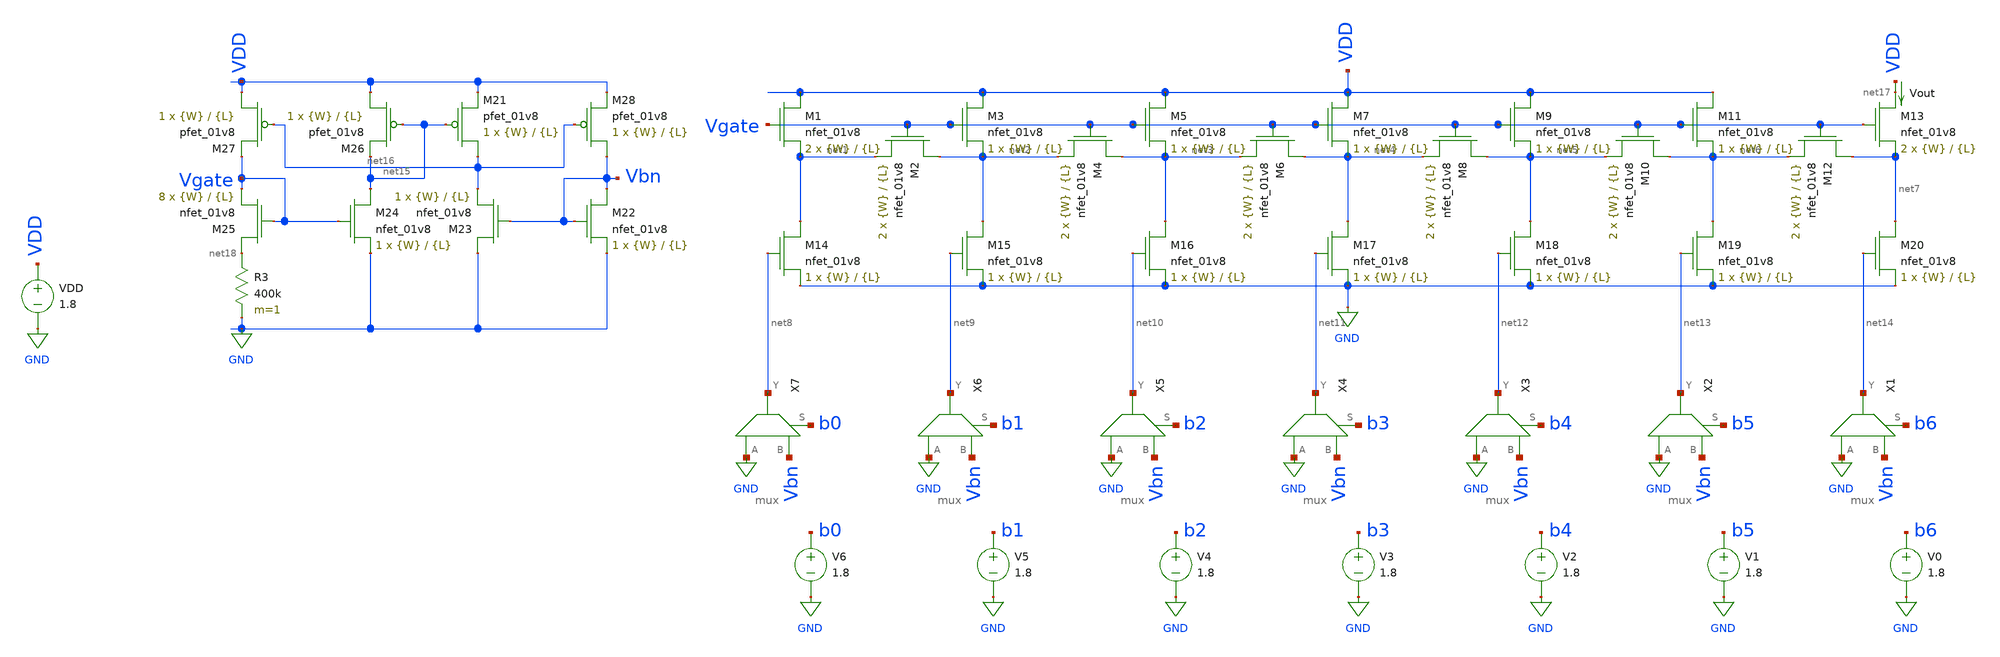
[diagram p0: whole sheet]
** sch_path: dac/schematics/misc/dac_output_current.sch
**.subckt dac_output_current
XM1 VDD Vgate net1 GND sky130_fd_pr__nfet_01v8 L={L} W={W} nf=1 ad='int((nf+1)/2) * W/nf * 0.29' as='int((nf+2)/2) * W/nf * 0.29'
+ pd='2*int((nf+1)/2) * (W/nf + 0.29)' ps='2*int((nf+2)/2) * (W/nf + 0.29)' nrd='0.29 / W' nrs='0.29 / W'
+ sa=0 sb=0 sd=0 mult=2 m=2
XM2 net2 Vgate net1 GND sky130_fd_pr__nfet_01v8 L={L} W={W} nf=1 ad='int((nf+1)/2) * W/nf * 0.29' as='int((nf+2)/2) * W/nf * 0.29'
+ pd='2*int((nf+1)/2) * (W/nf + 0.29)' ps='2*int((nf+2)/2) * (W/nf + 0.29)' nrd='0.29 / W' nrs='0.29 / W'
+ sa=0 sb=0 sd=0 mult=2 m=2
XM3 VDD Vgate net2 GND sky130_fd_pr__nfet_01v8 L={L} W={W} nf=1 ad='int((nf+1)/2) * W/nf * 0.29' as='int((nf+2)/2) * W/nf * 0.29'
+ pd='2*int((nf+1)/2) * (W/nf + 0.29)' ps='2*int((nf+2)/2) * (W/nf + 0.29)' nrd='0.29 / W' nrs='0.29 / W'
+ sa=0 sb=0 sd=0 mult=1 m=1
XM4 net3 Vgate net2 GND sky130_fd_pr__nfet_01v8 L={L} W={W} nf=1 ad='int((nf+1)/2) * W/nf * 0.29' as='int((nf+2)/2) * W/nf * 0.29'
+ pd='2*int((nf+1)/2) * (W/nf + 0.29)' ps='2*int((nf+2)/2) * (W/nf + 0.29)' nrd='0.29 / W' nrs='0.29 / W'
+ sa=0 sb=0 sd=0 mult=2 m=2
XM5 VDD Vgate net3 GND sky130_fd_pr__nfet_01v8 L={L} W={W} nf=1 ad='int((nf+1)/2) * W/nf * 0.29' as='int((nf+2)/2) * W/nf * 0.29'
+ pd='2*int((nf+1)/2) * (W/nf + 0.29)' ps='2*int((nf+2)/2) * (W/nf + 0.29)' nrd='0.29 / W' nrs='0.29 / W'
+ sa=0 sb=0 sd=0 mult=1 m=1
XM6 net4 Vgate net3 GND sky130_fd_pr__nfet_01v8 L={L} W={W} nf=1 ad='int((nf+1)/2) * W/nf * 0.29' as='int((nf+2)/2) * W/nf * 0.29'
+ pd='2*int((nf+1)/2) * (W/nf + 0.29)' ps='2*int((nf+2)/2) * (W/nf + 0.29)' nrd='0.29 / W' nrs='0.29 / W'
+ sa=0 sb=0 sd=0 mult=2 m=2
XM7 VDD Vgate net4 GND sky130_fd_pr__nfet_01v8 L={L} W={W} nf=1 ad='int((nf+1)/2) * W/nf * 0.29' as='int((nf+2)/2) * W/nf * 0.29'
+ pd='2*int((nf+1)/2) * (W/nf + 0.29)' ps='2*int((nf+2)/2) * (W/nf + 0.29)' nrd='0.29 / W' nrs='0.29 / W'
+ sa=0 sb=0 sd=0 mult=1 m=1
XM8 net5 Vgate net4 GND sky130_fd_pr__nfet_01v8 L={L} W={W} nf=1 ad='int((nf+1)/2) * W/nf * 0.29' as='int((nf+2)/2) * W/nf * 0.29'
+ pd='2*int((nf+1)/2) * (W/nf + 0.29)' ps='2*int((nf+2)/2) * (W/nf + 0.29)' nrd='0.29 / W' nrs='0.29 / W'
+ sa=0 sb=0 sd=0 mult=2 m=2
XM9 VDD Vgate net5 GND sky130_fd_pr__nfet_01v8 L={L} W={W} nf=1 ad='int((nf+1)/2) * W/nf * 0.29' as='int((nf+2)/2) * W/nf * 0.29'
+ pd='2*int((nf+1)/2) * (W/nf + 0.29)' ps='2*int((nf+2)/2) * (W/nf + 0.29)' nrd='0.29 / W' nrs='0.29 / W'
+ sa=0 sb=0 sd=0 mult=1 m=1
XM10 net6 Vgate net5 GND sky130_fd_pr__nfet_01v8 L={L} W={W} nf=1 ad='int((nf+1)/2) * W/nf * 0.29' as='int((nf+2)/2) * W/nf * 0.29'
+ pd='2*int((nf+1)/2) * (W/nf + 0.29)' ps='2*int((nf+2)/2) * (W/nf + 0.29)' nrd='0.29 / W' nrs='0.29 / W'
+ sa=0 sb=0 sd=0 mult=2 m=2
XM11 VDD Vgate net6 GND sky130_fd_pr__nfet_01v8 L={L} W={W} nf=1 ad='int((nf+1)/2) * W/nf * 0.29' as='int((nf+2)/2) * W/nf * 0.29'
+ pd='2*int((nf+1)/2) * (W/nf + 0.29)' ps='2*int((nf+2)/2) * (W/nf + 0.29)' nrd='0.29 / W' nrs='0.29 / W'
+ sa=0 sb=0 sd=0 mult=1 m=1
XM12 net7 Vgate net6 GND sky130_fd_pr__nfet_01v8 L={L} W={W} nf=1 ad='int((nf+1)/2) * W/nf * 0.29' as='int((nf+2)/2) * W/nf * 0.29'
+ pd='2*int((nf+1)/2) * (W/nf + 0.29)' ps='2*int((nf+2)/2) * (W/nf + 0.29)' nrd='0.29 / W' nrs='0.29 / W'
+ sa=0 sb=0 sd=0 mult=2 m=2
XM13 net17 Vgate net7 GND sky130_fd_pr__nfet_01v8 L={L} W={W} nf=1 ad='int((nf+1)/2) * W/nf * 0.29' as='int((nf+2)/2) * W/nf * 0.29'
+ pd='2*int((nf+1)/2) * (W/nf + 0.29)' ps='2*int((nf+2)/2) * (W/nf + 0.29)' nrd='0.29 / W' nrs='0.29 / W'
+ sa=0 sb=0 sd=0 mult=2 m=2
XM14 net1 net8 GND GND sky130_fd_pr__nfet_01v8 L={L} W={W} nf=1 ad='int((nf+1)/2) * W/nf * 0.29' as='int((nf+2)/2) * W/nf * 0.29'
+ pd='2*int((nf+1)/2) * (W/nf + 0.29)' ps='2*int((nf+2)/2) * (W/nf + 0.29)' nrd='0.29 / W' nrs='0.29 / W'
+ sa=0 sb=0 sd=0 mult=1 m=1
XM15 net2 net9 GND GND sky130_fd_pr__nfet_01v8 L={L} W={W} nf=1 ad='int((nf+1)/2) * W/nf * 0.29' as='int((nf+2)/2) * W/nf * 0.29'
+ pd='2*int((nf+1)/2) * (W/nf + 0.29)' ps='2*int((nf+2)/2) * (W/nf + 0.29)' nrd='0.29 / W' nrs='0.29 / W'
+ sa=0 sb=0 sd=0 mult=1 m=1
XM16 net3 net10 GND GND sky130_fd_pr__nfet_01v8 L={L} W={W} nf=1 ad='int((nf+1)/2) * W/nf * 0.29' as='int((nf+2)/2) * W/nf * 0.29'
+ pd='2*int((nf+1)/2) * (W/nf + 0.29)' ps='2*int((nf+2)/2) * (W/nf + 0.29)' nrd='0.29 / W' nrs='0.29 / W'
+ sa=0 sb=0 sd=0 mult=1 m=1
XM17 net4 net11 GND GND sky130_fd_pr__nfet_01v8 L={L} W={W} nf=1 ad='int((nf+1)/2) * W/nf * 0.29' as='int((nf+2)/2) * W/nf * 0.29'
+ pd='2*int((nf+1)/2) * (W/nf + 0.29)' ps='2*int((nf+2)/2) * (W/nf + 0.29)' nrd='0.29 / W' nrs='0.29 / W'
+ sa=0 sb=0 sd=0 mult=1 m=1
XM18 net5 net12 GND GND sky130_fd_pr__nfet_01v8 L={L} W={W} nf=1 ad='int((nf+1)/2) * W/nf * 0.29' as='int((nf+2)/2) * W/nf * 0.29'
+ pd='2*int((nf+1)/2) * (W/nf + 0.29)' ps='2*int((nf+2)/2) * (W/nf + 0.29)' nrd='0.29 / W' nrs='0.29 / W'
+ sa=0 sb=0 sd=0 mult=1 m=1
XM19 net6 net13 GND GND sky130_fd_pr__nfet_01v8 L={L} W={W} nf=1 ad='int((nf+1)/2) * W/nf * 0.29' as='int((nf+2)/2) * W/nf * 0.29'
+ pd='2*int((nf+1)/2) * (W/nf + 0.29)' ps='2*int((nf+2)/2) * (W/nf + 0.29)' nrd='0.29 / W' nrs='0.29 / W'
+ sa=0 sb=0 sd=0 mult=1 m=1
XM20 net7 net14 GND GND sky130_fd_pr__nfet_01v8 L={L} W={W} nf=1 ad='int((nf+1)/2) * W/nf * 0.29' as='int((nf+2)/2) * W/nf * 0.29'
+ pd='2*int((nf+1)/2) * (W/nf + 0.29)' ps='2*int((nf+2)/2) * (W/nf + 0.29)' nrd='0.29 / W' nrs='0.29 / W'
+ sa=0 sb=0 sd=0 mult=1 m=1
X1 GND Vbn net14 b6 mux
X2 GND Vbn net13 b5 mux
X3 GND Vbn net12 b4 mux
X4 GND Vbn net11 b3 mux
X5 GND Vbn net10 b2 mux
X6 GND Vbn net9 b1 mux
X7 GND Vbn net8 b0 mux
V0 b6 GND 1.8
V1 b5 GND 1.8
V2 b4 GND 1.8
V3 b3 GND 1.8
V4 b2 GND 1.8
V5 b1 GND 1.8
V6 b0 GND 1.8
Vout VDD net17 0
.save i(vout)
VDD VDD GND 1.8
R3 net18 GND 400k m=1
XM28 Vbn net16 VDD VDD sky130_fd_pr__pfet_01v8 L={L} W={W} nf=1 ad='int((nf+1)/2) * W/nf * 0.29' as='int((nf+2)/2) * W/nf * 0.29'
+ pd='2*int((nf+1)/2) * (W/nf + 0.29)' ps='2*int((nf+2)/2) * (W/nf + 0.29)' nrd='0.29 / W' nrs='0.29 / W'
+ sa=0 sb=0 sd=0 mult=1 m=1
XM21 net16 net15 VDD VDD sky130_fd_pr__pfet_01v8 L={L} W={W} nf=1 ad='int((nf+1)/2) * W/nf * 0.29' as='int((nf+2)/2) * W/nf * 0.29'
+ pd='2*int((nf+1)/2) * (W/nf + 0.29)' ps='2*int((nf+2)/2) * (W/nf + 0.29)' nrd='0.29 / W' nrs='0.29 / W'
+ sa=0 sb=0 sd=0 mult=1 m=1
XM26 VDD net15 net15 VDD sky130_fd_pr__pfet_01v8 L={L} W={W} nf=1 ad='int((nf+1)/2) * W/nf * 0.29' as='int((nf+2)/2) * W/nf * 0.29'
+ pd='2*int((nf+1)/2) * (W/nf + 0.29)' ps='2*int((nf+2)/2) * (W/nf + 0.29)' nrd='0.29 / W' nrs='0.29 / W'
+ sa=0 sb=0 sd=0 mult=1 m=1
XM27 VDD net16 Vgate VDD sky130_fd_pr__pfet_01v8 L={L} W={W} nf=1 ad='int((nf+1)/2) * W/nf * 0.29' as='int((nf+2)/2) * W/nf * 0.29'
+ pd='2*int((nf+1)/2) * (W/nf + 0.29)' ps='2*int((nf+2)/2) * (W/nf + 0.29)' nrd='0.29 / W' nrs='0.29 / W'
+ sa=0 sb=0 sd=0 mult=1 m=1
XM22 Vbn Vbn GND GND sky130_fd_pr__nfet_01v8 L={L} W={W} nf=1 ad='int((nf+1)/2) * W/nf * 0.29' as='int((nf+2)/2) * W/nf * 0.29'
+ pd='2*int((nf+1)/2) * (W/nf + 0.29)' ps='2*int((nf+2)/2) * (W/nf + 0.29)' nrd='0.29 / W' nrs='0.29 / W'
+ sa=0 sb=0 sd=0 mult=1 m=1
XM23 GND Vbn net16 GND sky130_fd_pr__nfet_01v8 L={L} W={W} nf=1 ad='int((nf+1)/2) * W/nf * 0.29' as='int((nf+2)/2) * W/nf * 0.29'
+ pd='2*int((nf+1)/2) * (W/nf + 0.29)' ps='2*int((nf+2)/2) * (W/nf + 0.29)' nrd='0.29 / W' nrs='0.29 / W'
+ sa=0 sb=0 sd=0 mult=1 m=1
XM24 net15 Vgate GND GND sky130_fd_pr__nfet_01v8 L={L} W={W} nf=1 ad='int((nf+1)/2) * W/nf * 0.29' as='int((nf+2)/2) * W/nf * 0.29'
+ pd='2*int((nf+1)/2) * (W/nf + 0.29)' ps='2*int((nf+2)/2) * (W/nf + 0.29)' nrd='0.29 / W' nrs='0.29 / W'
+ sa=0 sb=0 sd=0 mult=1 m=1
XM25 net18 Vgate Vgate GND sky130_fd_pr__nfet_01v8 L={L} W={W} nf=1 ad='int((nf+1)/2) * W/nf * 0.29'
+ as='int((nf+2)/2) * W/nf * 0.29' pd='2*int((nf+1)/2) * (W/nf + 0.29)' ps='2*int((nf+2)/2) * (W/nf + 0.29)'
+ nrd='0.29 / W' nrs='0.29 / W' sa=0 sb=0 sd=0 mult=8 m=8
**** begin user architecture code

.param W=1
.param L=0.5
.dc VDD 0 1.8 0.01
.save i(Vout) v(VDD) v(Vbn) v(Vgate)


.option wnflag=1
.param MC_SWITCH=0.0
.lib ~/skywater/skywater-pdk/libraries/sky130_fd_pr_ngspice/latest/models/sky130.lib.spice tt

**** end user architecture code
**.ends

* expanding   symbol:  /home/madvlsi/Documents/current-output-dac-vlsi/schematics/mux.sym # of
*+ pins=4
** sym_path: dac/schematics/mux.sym
** sch_path: dac/schematics/mux.sch
.subckt mux A B Y S
*.ipin A
*.ipin B
*.ipin S
*.opin Y
XM1 A S Y VDD sky130_fd_pr__pfet_01v8 L=0.15 W=1 nf=1 ad='int((nf+1)/2) * W/nf * 0.29' as='int((nf+2)/2) * W/nf * 0.29'
+ pd='2*int((nf+1)/2) * (W/nf + 0.29)' ps='2*int((nf+2)/2) * (W/nf + 0.29)' nrd='0.29 / W' nrs='0.29 / W'
+ sa=0 sb=0 sd=0 mult=1 m=1
XM3 net1 S VDD VDD sky130_fd_pr__pfet_01v8 L=0.15 W=1 nf=1 ad='int((nf+1)/2) * W/nf * 0.29' as='int((nf+2)/2) * W/nf * 0.29'
+ pd='2*int((nf+1)/2) * (W/nf + 0.29)' ps='2*int((nf+2)/2) * (W/nf + 0.29)' nrd='0.29 / W' nrs='0.29 / W'
+ sa=0 sb=0 sd=0 mult=1 m=1
XM4 net1 S GND GND sky130_fd_pr__nfet_01v8 L=0.15 W=1 nf=1 ad='int((nf+1)/2) * W/nf * 0.29' as='int((nf+2)/2) * W/nf * 0.29'
+ pd='2*int((nf+1)/2) * (W/nf + 0.29)' ps='2*int((nf+2)/2) * (W/nf + 0.29)' nrd='0.29 / W' nrs='0.29 / W'
+ sa=0 sb=0 sd=0 mult=1 m=1
XM5 A net1 Y GND sky130_fd_pr__nfet_01v8 L=0.15 W=1 nf=1 ad='int((nf+1)/2) * W/nf * 0.29' as='int((nf+2)/2) * W/nf * 0.29'
+ pd='2*int((nf+1)/2) * (W/nf + 0.29)' ps='2*int((nf+2)/2) * (W/nf + 0.29)' nrd='0.29 / W' nrs='0.29 / W'
+ sa=0 sb=0 sd=0 mult=1 m=1
XM2 B net1 Y VDD sky130_fd_pr__pfet_01v8 L=0.15 W=1 nf=1 ad='int((nf+1)/2) * W/nf * 0.29' as='int((nf+2)/2) * W/nf * 0.29'
+ pd='2*int((nf+1)/2) * (W/nf + 0.29)' ps='2*int((nf+2)/2) * (W/nf + 0.29)' nrd='0.29 / W' nrs='0.29 / W'
+ sa=0 sb=0 sd=0 mult=1 m=1
XM6 B S Y GND sky130_fd_pr__nfet_01v8 L=0.15 W=1 nf=1 ad='int((nf+1)/2) * W/nf * 0.29' as='int((nf+2)/2) * W/nf * 0.29'
+ pd='2*int((nf+1)/2) * (W/nf + 0.29)' ps='2*int((nf+2)/2) * (W/nf + 0.29)' nrd='0.29 / W' nrs='0.29 / W'
+ sa=0 sb=0 sd=0 mult=1 m=1
.ends

.GLOBAL GND
.GLOBAL VDD
.end
